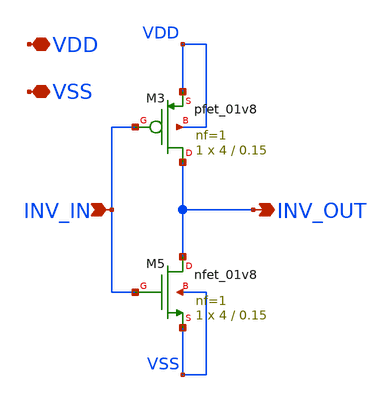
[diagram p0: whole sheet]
** sch_path: xschem/untitled-3.sch
**.subckt untitled-3 INV_IN INV_OUT VDD VSS
*.ipin INV_IN
*.opin INV_OUT
*.iopin VDD
*.iopin VSS
XM3 INV_OUT INV_IN VDD VDD sky130_fd_pr__pfet_01v8 L=0.15 W=4 nf=1 ad='int((nf+1)/2) * W/nf * 0.29' as='int((nf+2)/2) * W/nf * 0.29'
+ pd='2*int((nf+1)/2) * (W/nf + 0.29)' ps='2*int((nf+2)/2) * (W/nf + 0.29)' nrd='0.29 / W' nrs='0.29 / W'
+ sa=0 sb=0 sd=0 mult=1 m=1
XM5 INV_OUT INV_IN VSS VSS sky130_fd_pr__nfet_01v8 L=0.15 W=4 nf=1 ad='int((nf+1)/2) * W/nf * 0.29' as='int((nf+2)/2) * W/nf * 0.29'
+ pd='2*int((nf+1)/2) * (W/nf + 0.29)' ps='2*int((nf+2)/2) * (W/nf + 0.29)' nrd='0.29 / W' nrs='0.29 / W'
+ sa=0 sb=0 sd=0 mult=1 m=1
**.ends
.end
